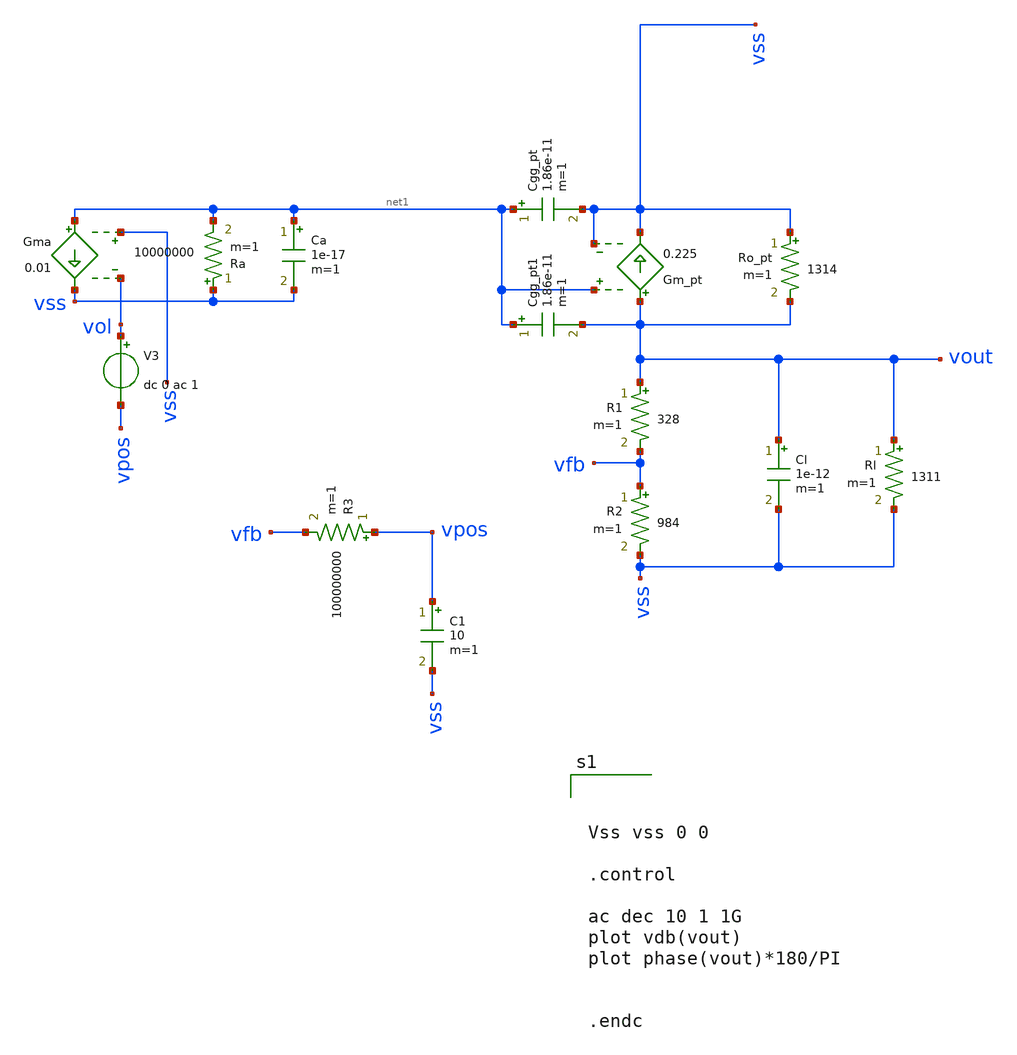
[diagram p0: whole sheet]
** sch_path: test-python/Tesis_notebooks/xschem/ldo_ol_ss_tb.sch
**.subckt ldo_ol_ss_tb
R3 vpos vfb 100000000 m=1
C1 vpos vss 10 m=1
Ro_pt vss vout 1314 m=1
Gm_pt vout vss net1 vss 0.225
R1 vout vfb 328 m=1
R2 vfb vss 984 m=1
Gma net1 vss vss vol 0.01
Ra vss net1 10000000 m=1
Rl vout vss 1311 m=1
Cgg_pt net1 vss 1.86e-11 m=1
Ca net1 vss 1e-17 m=1
Cl vout vss 1e-12 m=1
V3 vol vpos dc 0 ac 1
Cgg_pt1 net1 vout 1.86e-11 m=1
**** begin user architecture code



Vss vss 0 0

.control

ac dec 10 1 1G
plot vdb(vout)
plot phase(vout)*180/PI


.endc



**** end user architecture code
**.ends
.end
